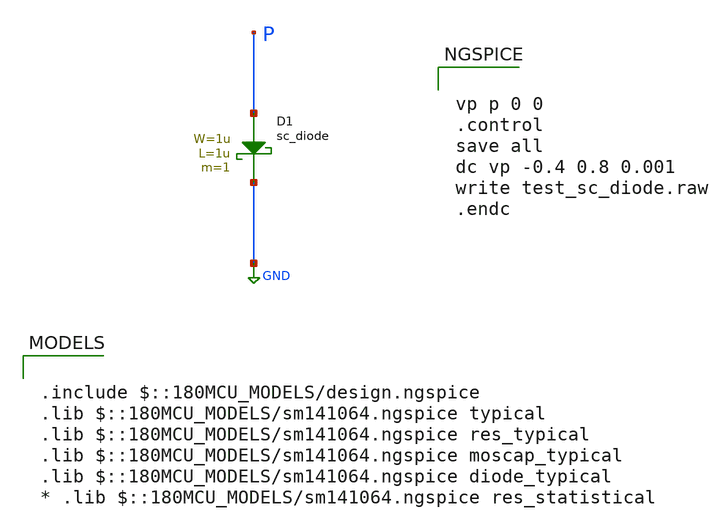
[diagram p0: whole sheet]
** sch_path: gf180mcuD/xschem_libs/gf180mcu_tests/test_sc_diode/schematic/test_sc_diode.sch
* Copyright 2022 GlobalFoundries PDK Authors
* Licensed under the Apache License, Version 2.0 (the "License");
* you may not use this file except in compliance with the License.
* You may obtain a copy of the License at
* https://www.apache.org/licenses/LICENSE-2.0
* Unless required by applicable law or agreed to in writing, software
* distributed under the License is distributed on an "AS IS" BASIS,
* WITHOUT WARRANTIES OR CONDITIONS OF ANY KIND, either express or implied.
* See the License for the specific language governing permissions and
* limitations under the License.
**.subckt test_sc_diode
D1 P GND sc_diode area='1u * 1u ' pj='2*1u + 2*1u ' m=1
**** begin user architecture code

.include $::180MCU_MODELS/design.ngspice
.lib $::180MCU_MODELS/sm141064.ngspice typical
.lib $::180MCU_MODELS/sm141064.ngspice res_typical
.lib $::180MCU_MODELS/sm141064.ngspice moscap_typical
.lib $::180MCU_MODELS/sm141064.ngspice diode_typical
* .lib $::180MCU_MODELS/sm141064.ngspice res_statistical



vp p 0 0
.control
save all
dc vp -0.4 0.8 0.001
write test_sc_diode.raw
.endc


**** end user architecture code
**.ends
.GLOBAL GND
.end
